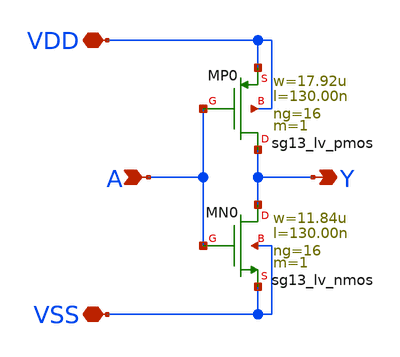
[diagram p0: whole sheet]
** sch_path: xschem/inv_16.sch
**.subckt inv_16 Y A VDD VSS
*.opin Y
*.ipin A
*.iopin VDD
*.iopin VSS
XMN0 Y A VSS VSS sg13_lv_nmos w=11.84u l=130.00n ng=16 m=1 mm_ok=1
XMP0 Y A VDD VDD sg13_lv_pmos w=17.92u l=130.00n ng=16 m=1 mm_ok=1
**.ends
.end
